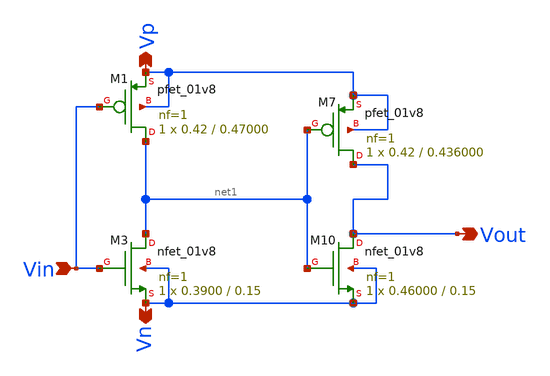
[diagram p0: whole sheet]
** sch_path: xschem/Vth_sch/Symbol/th06.sch
**.subckt th06 Vn Vp Vin Vout
*.opin Vn
*.opin Vp
*.ipin Vin
*.opin Vout
XM7 Vout net1 Vp Vp sky130_fd_pr__pfet_01v8 L=0.436000 W=0.42 nf=1 ad='int((nf+1)/2) * W/nf * 0.29' as='int((nf+2)/2) * W/nf * 0.29'
+ pd='2*int((nf+1)/2) * (W/nf + 0.29)' ps='2*int((nf+2)/2) * (W/nf + 0.29)' nrd='0.29 / W' nrs='0.29 / W'
+ sa=0 sb=0 sd=0 mult=1 m=1
XM10 Vout net1 Vn Vn sky130_fd_pr__nfet_01v8 L=0.15 W=0.46000 nf=1 ad='int((nf+1)/2) * W/nf * 0.29' as='int((nf+2)/2) * W/nf * 0.29'
+ pd='2*int((nf+1)/2) * (W/nf + 0.29)' ps='2*int((nf+2)/2) * (W/nf + 0.29)' nrd='0.29 / W' nrs='0.29 / W'
+ sa=0 sb=0 sd=0 mult=1 m=1
XM1 net1 Vin Vp Vp sky130_fd_pr__pfet_01v8 L=0.47000 W=0.42 nf=1 ad='int((nf+1)/2) * W/nf * 0.29' as='int((nf+2)/2) * W/nf * 0.29'
+ pd='2*int((nf+1)/2) * (W/nf + 0.29)' ps='2*int((nf+2)/2) * (W/nf + 0.29)' nrd='0.29 / W' nrs='0.29 / W'
+ sa=0 sb=0 sd=0 mult=1 m=1
XM3 net1 Vin Vn Vn sky130_fd_pr__nfet_01v8 L=0.15 W=0.3900 nf=1 ad='int((nf+1)/2) * W/nf * 0.29' as='int((nf+2)/2) * W/nf * 0.29'
+ pd='2*int((nf+1)/2) * (W/nf + 0.29)' ps='2*int((nf+2)/2) * (W/nf + 0.29)' nrd='0.29 / W' nrs='0.29 / W'
+ sa=0 sb=0 sd=0 mult=1 m=1
**.ends
.end
